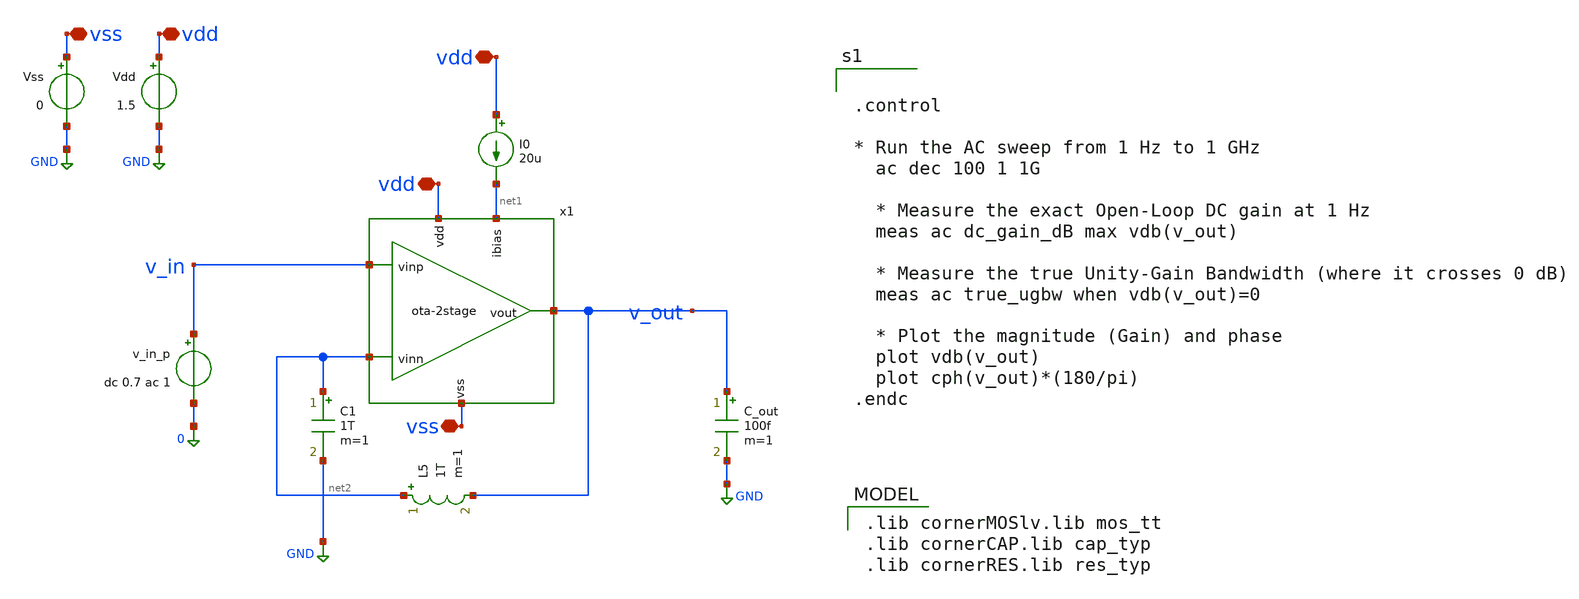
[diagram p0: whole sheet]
** sch_path: testbench/ota-2stage_tb-gain.sch
**.subckt ota-2stage_tb-gain vss vdd vdd vdd vss
*.iopin vss
*.iopin vdd
*.iopin vdd
*.iopin vdd
*.iopin vss
x1 vdd net1 net2 v_out v_in vss ota-2stage
Vdd vdd GND 1.5
Vss vss GND 0
I0 vdd net1 20u
v_in_p v_in 0 dc 0.7 ac 1
C_out v_out GND 100f m=1
L5 net2 v_out 1T m=1
C1 net2 GND 1T m=1
**** begin user architecture code


.control

* Run the AC sweep from 1 Hz to 1 GHz
  ac dec 100 1 1G

  * Measure the exact Open-Loop DC gain at 1 Hz
  meas ac dc_gain_dB max vdb(v_out)

  * Measure the true Unity-Gain Bandwidth (where it crosses 0 dB)
  meas ac true_ugbw when vdb(v_out)=0

  * Plot the magnitude (Gain) and phase
  plot vdb(v_out)
  plot cph(v_out)*(180/pi)
.endc


 .lib cornerMOSlv.lib mos_tt
.lib cornerCAP.lib cap_typ
.lib cornerRES.lib res_typ

**** end user architecture code
**.ends
.GLOBAL GND
.end
